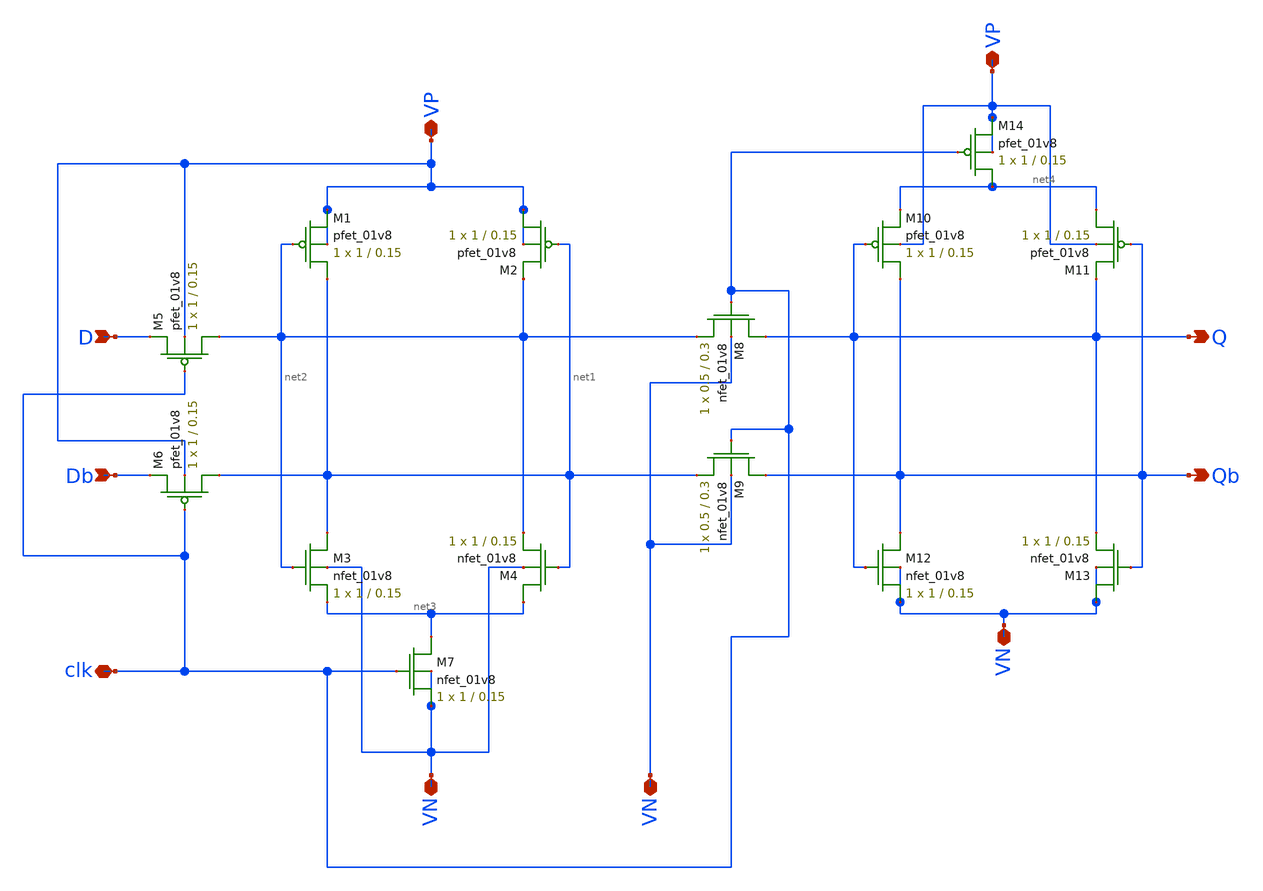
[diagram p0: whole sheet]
** sch_path: Mini_Project_2/Shift_reg/schematics/CSRL_latch.sch
**.subckt CSRL_latch D Db Q Qb clk VP VN VN VP VN
*.ipin D
*.ipin Db
*.opin Q
*.opin Qb
*.iopin clk
*.iopin VP
*.iopin VN
*.iopin VN
*.iopin VP
*.iopin VN
XM5 net2 clk D VP sky130_fd_pr__pfet_01v8 L=0.15 W=1 nf=1 ad='int((nf+1)/2) * W/nf * 0.29' as='int((nf+2)/2) * W/nf * 0.29'
+ pd='2*int((nf+1)/2) * (W/nf + 0.29)' ps='2*int((nf+2)/2) * (W/nf + 0.29)' nrd='0.29 / W' nrs='0.29 / W'
+ sa=0 sb=0 sd=0 mult=1 m=1
XM6 net1 clk Db VP sky130_fd_pr__pfet_01v8 L=0.15 W=1 nf=1 ad='int((nf+1)/2) * W/nf * 0.29' as='int((nf+2)/2) * W/nf * 0.29'
+ pd='2*int((nf+1)/2) * (W/nf + 0.29)' ps='2*int((nf+2)/2) * (W/nf + 0.29)' nrd='0.29 / W' nrs='0.29 / W'
+ sa=0 sb=0 sd=0 mult=1 m=1
XM1 net1 net2 VP VP sky130_fd_pr__pfet_01v8 L=0.15 W=1 nf=1 ad='int((nf+1)/2) * W/nf * 0.29' as='int((nf+2)/2) * W/nf * 0.29'
+ pd='2*int((nf+1)/2) * (W/nf + 0.29)' ps='2*int((nf+2)/2) * (W/nf + 0.29)' nrd='0.29 / W' nrs='0.29 / W'
+ sa=0 sb=0 sd=0 mult=1 m=1
XM2 VP net1 net2 VP sky130_fd_pr__pfet_01v8 L=0.15 W=1 nf=1 ad='int((nf+1)/2) * W/nf * 0.29' as='int((nf+2)/2) * W/nf * 0.29'
+ pd='2*int((nf+1)/2) * (W/nf + 0.29)' ps='2*int((nf+2)/2) * (W/nf + 0.29)' nrd='0.29 / W' nrs='0.29 / W'
+ sa=0 sb=0 sd=0 mult=1 m=1
XM3 net1 net2 net3 VN sky130_fd_pr__nfet_01v8 L=0.15 W=1 nf=1 ad='int((nf+1)/2) * W/nf * 0.29' as='int((nf+2)/2) * W/nf * 0.29'
+ pd='2*int((nf+1)/2) * (W/nf + 0.29)' ps='2*int((nf+2)/2) * (W/nf + 0.29)' nrd='0.29 / W' nrs='0.29 / W'
+ sa=0 sb=0 sd=0 mult=1 m=1
XM4 net3 net1 net2 VN sky130_fd_pr__nfet_01v8 L=0.15 W=1 nf=1 ad='int((nf+1)/2) * W/nf * 0.29' as='int((nf+2)/2) * W/nf * 0.29'
+ pd='2*int((nf+1)/2) * (W/nf + 0.29)' ps='2*int((nf+2)/2) * (W/nf + 0.29)' nrd='0.29 / W' nrs='0.29 / W'
+ sa=0 sb=0 sd=0 mult=1 m=1
XM7 net3 clk VN VN sky130_fd_pr__nfet_01v8 L=0.15 W=1 nf=1 ad='int((nf+1)/2) * W/nf * 0.29' as='int((nf+2)/2) * W/nf * 0.29'
+ pd='2*int((nf+1)/2) * (W/nf + 0.29)' ps='2*int((nf+2)/2) * (W/nf + 0.29)' nrd='0.29 / W' nrs='0.29 / W'
+ sa=0 sb=0 sd=0 mult=1 m=1
XM8 Q clk net2 VN sky130_fd_pr__nfet_01v8 L=0.3 W=0.5 nf=1 ad='int((nf+1)/2) * W/nf * 0.29' as='int((nf+2)/2) * W/nf * 0.29'
+ pd='2*int((nf+1)/2) * (W/nf + 0.29)' ps='2*int((nf+2)/2) * (W/nf + 0.29)' nrd='0.29 / W' nrs='0.29 / W'
+ sa=0 sb=0 sd=0 mult=1 m=1
XM9 Qb clk net1 VN sky130_fd_pr__nfet_01v8 L=0.3 W=0.5 nf=1 ad='int((nf+1)/2) * W/nf * 0.29' as='int((nf+2)/2) * W/nf * 0.29'
+ pd='2*int((nf+1)/2) * (W/nf + 0.29)' ps='2*int((nf+2)/2) * (W/nf + 0.29)' nrd='0.29 / W' nrs='0.29 / W'
+ sa=0 sb=0 sd=0 mult=1 m=1
XM12 Qb Q VN VN sky130_fd_pr__nfet_01v8 L=0.15 W=1 nf=1 ad='int((nf+1)/2) * W/nf * 0.29' as='int((nf+2)/2) * W/nf * 0.29'
+ pd='2*int((nf+1)/2) * (W/nf + 0.29)' ps='2*int((nf+2)/2) * (W/nf + 0.29)' nrd='0.29 / W' nrs='0.29 / W'
+ sa=0 sb=0 sd=0 mult=1 m=1
XM13 VN Qb Q VN sky130_fd_pr__nfet_01v8 L=0.15 W=1 nf=1 ad='int((nf+1)/2) * W/nf * 0.29' as='int((nf+2)/2) * W/nf * 0.29'
+ pd='2*int((nf+1)/2) * (W/nf + 0.29)' ps='2*int((nf+2)/2) * (W/nf + 0.29)' nrd='0.29 / W' nrs='0.29 / W'
+ sa=0 sb=0 sd=0 mult=1 m=1
XM10 Qb Q net4 VP sky130_fd_pr__pfet_01v8 L=0.15 W=1 nf=1 ad='int((nf+1)/2) * W/nf * 0.29' as='int((nf+2)/2) * W/nf * 0.29'
+ pd='2*int((nf+1)/2) * (W/nf + 0.29)' ps='2*int((nf+2)/2) * (W/nf + 0.29)' nrd='0.29 / W' nrs='0.29 / W'
+ sa=0 sb=0 sd=0 mult=1 m=1
XM11 net4 Qb Q VP sky130_fd_pr__pfet_01v8 L=0.15 W=1 nf=1 ad='int((nf+1)/2) * W/nf * 0.29' as='int((nf+2)/2) * W/nf * 0.29'
+ pd='2*int((nf+1)/2) * (W/nf + 0.29)' ps='2*int((nf+2)/2) * (W/nf + 0.29)' nrd='0.29 / W' nrs='0.29 / W'
+ sa=0 sb=0 sd=0 mult=1 m=1
XM14 net4 clk VP VP sky130_fd_pr__pfet_01v8 L=0.15 W=1 nf=1 ad='int((nf+1)/2) * W/nf * 0.29' as='int((nf+2)/2) * W/nf * 0.29'
+ pd='2*int((nf+1)/2) * (W/nf + 0.29)' ps='2*int((nf+2)/2) * (W/nf + 0.29)' nrd='0.29 / W' nrs='0.29 / W'
+ sa=0 sb=0 sd=0 mult=1 m=1
**.ends
.end
